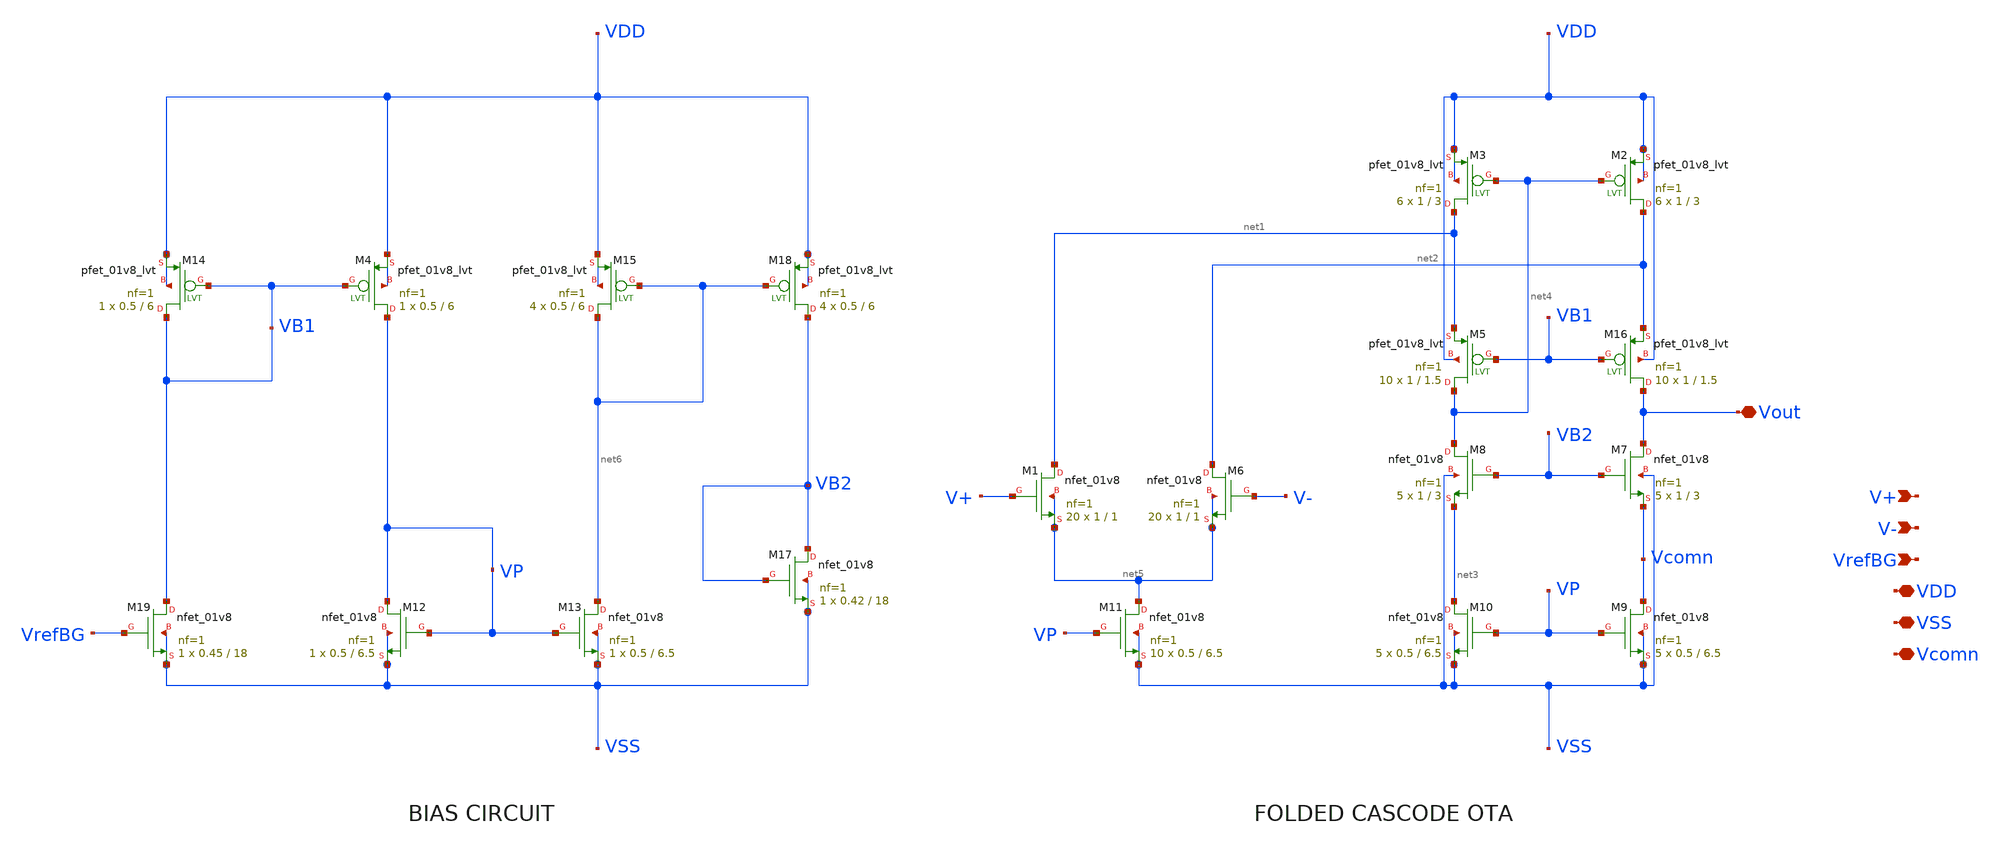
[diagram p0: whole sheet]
** sch_path: openfasoc/generators/curref-gen/sch/Folded_cascode.sch
**.subckt Folded_cascode V+ V- VrefBG VDD VSS Vout Vcomn
*.ipin V+
*.ipin V-
*.ipin VrefBG
*.iopin VDD
*.iopin VSS
*.iopin Vout
*.iopin Vcomn
XM6 net2 V- net5 net5 sky130_fd_pr__nfet_01v8 L=1 W=1 nf=1 ad='int((nf+1)/2) * W/nf * 0.29' as='int((nf+2)/2) * W/nf * 0.29'
+ pd='2*int((nf+1)/2) * (W/nf + 0.29)' ps='2*int((nf+2)/2) * (W/nf + 0.29)' nrd='0.29 / W' nrs='0.29 / W'
+ sa=0 sb=0 sd=0 mult=20 m=20
XM7 Vout VB2 Vcomn VSS sky130_fd_pr__nfet_01v8 L=3 W=1 nf=1 ad='int((nf+1)/2) * W/nf * 0.29' as='int((nf+2)/2) * W/nf * 0.29'
+ pd='2*int((nf+1)/2) * (W/nf + 0.29)' ps='2*int((nf+2)/2) * (W/nf + 0.29)' nrd='0.29 / W' nrs='0.29 / W'
+ sa=0 sb=0 sd=0 mult=5 m=5
XM8 net4 VB2 net3 VSS sky130_fd_pr__nfet_01v8 L=3 W=1 nf=1 ad='int((nf+1)/2) * W/nf * 0.29' as='int((nf+2)/2) * W/nf * 0.29'
+ pd='2*int((nf+1)/2) * (W/nf + 0.29)' ps='2*int((nf+2)/2) * (W/nf + 0.29)' nrd='0.29 / W' nrs='0.29 / W'
+ sa=0 sb=0 sd=0 mult=5 m=5
XM9 Vcomn VP VSS VSS sky130_fd_pr__nfet_01v8 L=6.5 W=0.5 nf=1 ad='int((nf+1)/2) * W/nf * 0.29' as='int((nf+2)/2) * W/nf * 0.29'
+ pd='2*int((nf+1)/2) * (W/nf + 0.29)' ps='2*int((nf+2)/2) * (W/nf + 0.29)' nrd='0.29 / W' nrs='0.29 / W'
+ sa=0 sb=0 sd=0 mult=5 m=5
XM10 net3 VP VSS VSS sky130_fd_pr__nfet_01v8 L=6.5 W=0.5 nf=1 ad='int((nf+1)/2) * W/nf * 0.29' as='int((nf+2)/2) * W/nf * 0.29'
+ pd='2*int((nf+1)/2) * (W/nf + 0.29)' ps='2*int((nf+2)/2) * (W/nf + 0.29)' nrd='0.29 / W' nrs='0.29 / W'
+ sa=0 sb=0 sd=0 mult=5 m=5
XM11 net5 VP VSS VSS sky130_fd_pr__nfet_01v8 L=6.5 W=0.5 nf=1 ad='int((nf+1)/2) * W/nf * 0.29' as='int((nf+2)/2) * W/nf * 0.29'
+ pd='2*int((nf+1)/2) * (W/nf + 0.29)' ps='2*int((nf+2)/2) * (W/nf + 0.29)' nrd='0.29 / W' nrs='0.29 / W'
+ sa=0 sb=0 sd=0 mult=10 m=10
XM1 net1 V+ net5 net5 sky130_fd_pr__nfet_01v8 L=1 W=1 nf=1 ad='int((nf+1)/2) * W/nf * 0.29' as='int((nf+2)/2) * W/nf * 0.29'
+ pd='2*int((nf+1)/2) * (W/nf + 0.29)' ps='2*int((nf+2)/2) * (W/nf + 0.29)' nrd='0.29 / W' nrs='0.29 / W'
+ sa=0 sb=0 sd=0 mult=20 m=20
XM12 VP VP VSS VSS sky130_fd_pr__nfet_01v8 L=6.5 W=0.5 nf=1 ad='int((nf+1)/2) * W/nf * 0.29' as='int((nf+2)/2) * W/nf * 0.29'
+ pd='2*int((nf+1)/2) * (W/nf + 0.29)' ps='2*int((nf+2)/2) * (W/nf + 0.29)' nrd='0.29 / W' nrs='0.29 / W'
+ sa=0 sb=0 sd=0 mult=1 m=1
XM13 net6 VP VSS VSS sky130_fd_pr__nfet_01v8 L=6.5 W=0.5 nf=1 ad='int((nf+1)/2) * W/nf * 0.29' as='int((nf+2)/2) * W/nf * 0.29'
+ pd='2*int((nf+1)/2) * (W/nf + 0.29)' ps='2*int((nf+2)/2) * (W/nf + 0.29)' nrd='0.29 / W' nrs='0.29 / W'
+ sa=0 sb=0 sd=0 mult=1 m=1
XM17 VB2 VB2 VSS VSS sky130_fd_pr__nfet_01v8 L=18 W=0.42 nf=1 ad='int((nf+1)/2) * W/nf * 0.29' as='int((nf+2)/2) * W/nf * 0.29'
+ pd='2*int((nf+1)/2) * (W/nf + 0.29)' ps='2*int((nf+2)/2) * (W/nf + 0.29)' nrd='0.29 / W' nrs='0.29 / W'
+ sa=0 sb=0 sd=0 mult=1 m=1
XM18 VB2 net6 VDD VDD sky130_fd_pr__pfet_01v8_lvt L=6 W=0.5 nf=1 ad='int((1 + 1)/2) * 0.5 / 1 * 0.29'
+ as='int((1 + 2)/2) * 0.5 / 1 * 0.29' pd='2*int((1 + 1)/2) * (0.5 / 1 + 0.29)' ps='2*int((1 + 2)/2) * (0.5 / 1 + 0.29)'
+ nrd='0.29 / 0.5 ' nrs='0.29 / 0.5 ' sa=0 sb=0 sd=0 mult=4 m=4
XM15 net6 net6 VDD VDD sky130_fd_pr__pfet_01v8_lvt L=6 W=0.5 nf=1 ad='int((1 + 1)/2) * 0.5 / 1 * 0.29'
+ as='int((1 + 2)/2) * 0.5 / 1 * 0.29' pd='2*int((1 + 1)/2) * (0.5 / 1 + 0.29)' ps='2*int((1 + 2)/2) * (0.5 / 1 + 0.29)'
+ nrd='0.29 / 0.5 ' nrs='0.29 / 0.5 ' sa=0 sb=0 sd=0 mult=4 m=4
XM3 net1 net4 VDD VDD sky130_fd_pr__pfet_01v8_lvt L=3 W=1 nf=1 ad='int((1 + 1)/2) * 1 / 1 * 0.29' as='int((1 + 2)/2) * 1 / 1 * 0.29'
+ pd='2*int((1 + 1)/2) * (1 / 1 + 0.29)' ps='2*int((1 + 2)/2) * (1 / 1 + 0.29)' nrd='0.29 / 1 ' nrs='0.29 / 1 '
+ sa=0 sb=0 sd=0 mult=6 m=6
XM2 net2 net4 VDD VDD sky130_fd_pr__pfet_01v8_lvt L=3 W=1 nf=1 ad='int((1 + 1)/2) * 1 / 1 * 0.29' as='int((1 + 2)/2) * 1 / 1 * 0.29'
+ pd='2*int((1 + 1)/2) * (1 / 1 + 0.29)' ps='2*int((1 + 2)/2) * (1 / 1 + 0.29)' nrd='0.29 / 1 ' nrs='0.29 / 1 '
+ sa=0 sb=0 sd=0 mult=6 m=6
XM5 net4 VB1 net1 VDD sky130_fd_pr__pfet_01v8_lvt L=1.5 W=1 nf=1 ad='int((1 + 1)/2) * 1 / 1 * 0.29' as='int((1 + 2)/2) * 1 / 1 * 0.29'
+ pd='2*int((1 + 1)/2) * (1 / 1 + 0.29)' ps='2*int((1 + 2)/2) * (1 / 1 + 0.29)' nrd='0.29 / 1 ' nrs='0.29 / 1 '
+ sa=0 sb=0 sd=0 mult=10 m=10
XM16 Vout VB1 net2 VDD sky130_fd_pr__pfet_01v8_lvt L=1.5 W=1 nf=1 ad='int((1 + 1)/2) * 1 / 1 * 0.29'
+ as='int((1 + 2)/2) * 1 / 1 * 0.29' pd='2*int((1 + 1)/2) * (1 / 1 + 0.29)' ps='2*int((1 + 2)/2) * (1 / 1 + 0.29)'
+ nrd='0.29 / 1 ' nrs='0.29 / 1 ' sa=0 sb=0 sd=0 mult=10 m=10
XM4 VP VB1 VDD VDD sky130_fd_pr__pfet_01v8_lvt L=6 W=0.5 nf=1 ad='int((1 + 1)/2) * 0.5 / 1 * 0.29' as='int((1 + 2)/2) * 0.5 / 1 * 0.29'
+ pd='2*int((1 + 1)/2) * (0.5 / 1 + 0.29)' ps='2*int((1 + 2)/2) * (0.5 / 1 + 0.29)' nrd='0.29 / 0.5 ' nrs='0.29 / 0.5 '
+ sa=0 sb=0 sd=0 mult=1 m=1
XM14 VB1 VB1 VDD VDD sky130_fd_pr__pfet_01v8_lvt L=6 W=0.5 nf=1 ad='int((1 + 1)/2) * 0.5 / 1 * 0.29'
+ as='int((1 + 2)/2) * 0.5 / 1 * 0.29' pd='2*int((1 + 1)/2) * (0.5 / 1 + 0.29)' ps='2*int((1 + 2)/2) * (0.5 / 1 + 0.29)'
+ nrd='0.29 / 0.5 ' nrs='0.29 / 0.5 ' sa=0 sb=0 sd=0 mult=1 m=1
XM19 VB1 VrefBG VSS VSS sky130_fd_pr__nfet_01v8 L=18 W=0.45 nf=1 ad='int((nf+1)/2) * W/nf * 0.29' as='int((nf+2)/2) * W/nf * 0.29'
+ pd='2*int((nf+1)/2) * (W/nf + 0.29)' ps='2*int((nf+2)/2) * (W/nf + 0.29)' nrd='0.29 / W' nrs='0.29 / W'
+ sa=0 sb=0 sd=0 mult=1 m=1
**.ends
.end
